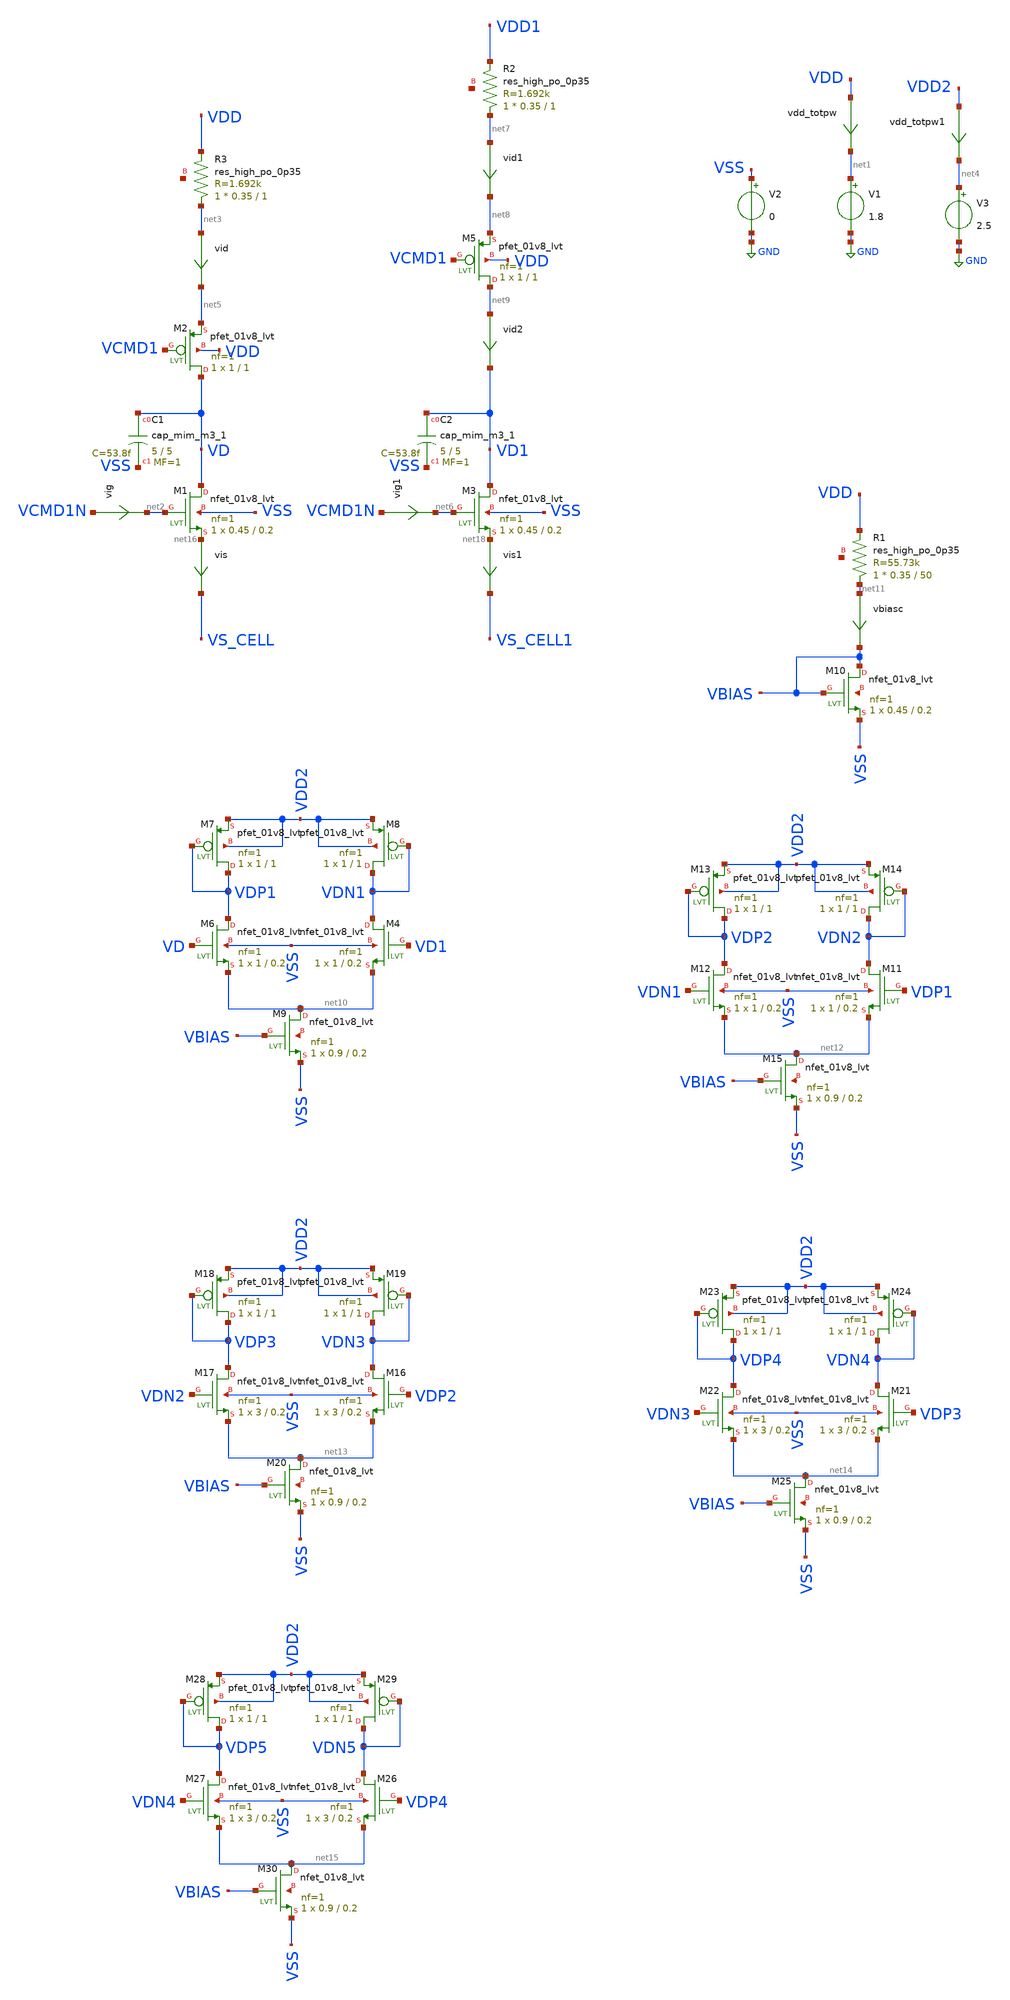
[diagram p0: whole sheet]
** sch_path: xschem/tb_em_dram_cell_sourcecap1.sch
**.subckt tb_em_dram_cell_sourcecap1
V1 net1 GND 1.8
V2 VSS GND 0
vdd_totpw VDD net1 0
.save i(vdd_totpw)
vis net16 VS_CELL 0
.save i(vis)
XR3 net3 VDD net17 sky130_fd_pr__res_high_po_0p35 L=1 mult=1 m=1
vig VCMD1N net2 0
.save i(vig)
vid net3 net5 0
.save i(vid)
XC1 VD VSS sky130_fd_pr__cap_mim_m3_1 W=5 L=5 MF=1 m=1
V3 net4 GND 2.5
vdd_totpw1 VDD2 net4 0
.save i(vdd_totpw1)
XM2 VD VCMD1 net5 VDD sky130_fd_pr__pfet_01v8_lvt L=1 W=1 nf=1 ad='int((nf+1)/2) * W/nf * 0.29' as='int((nf+2)/2) * W/nf * 0.29'
+ pd='2*int((nf+1)/2) * (W/nf + 0.29)' ps='2*int((nf+2)/2) * (W/nf + 0.29)' nrd='0.29 / W' nrs='0.29 / W'
+ sa=0 sb=0 sd=0 mult=1 m=1
vis1 net18 VS_CELL1 0
.save i(vis1)
XR2 net7 VDD1 net19 sky130_fd_pr__res_high_po_0p35 L=1 mult=1 m=1
vig1 VCMD1N net6 0
.save i(vig1)
vid1 net7 net8 0
.save i(vid1)
XC2 VD1 VSS sky130_fd_pr__cap_mim_m3_1 W=5 L=5 MF=1 m=1
XM5 net9 VCMD1 net8 VDD sky130_fd_pr__pfet_01v8_lvt L=1 W=1 nf=1 ad='int((nf+1)/2) * W/nf * 0.29' as='int((nf+2)/2) * W/nf * 0.29'
+ pd='2*int((nf+1)/2) * (W/nf + 0.29)' ps='2*int((nf+2)/2) * (W/nf + 0.29)' nrd='0.29 / W' nrs='0.29 / W'
+ sa=0 sb=0 sd=0 mult=1 m=1
vid2 net9 VD1 0
.save i(vid2)
XM1 VD net2 net16 VSS sky130_fd_pr__nfet_01v8_lvt L=0.2 W=0.45 nf=1 ad=0.4 as=0.4 pd='2*int((nf+1)/2) * (W/nf + 0.29)'
+ ps='2*int((nf+2)/2) * (W/nf + 0.29)' nrd='0.29 / W' nrs='0.29 / W' sa=0 sb=0 sd=0 mult=1 m=1
XM3 VD1 net6 net18 VSS sky130_fd_pr__nfet_01v8_lvt L=0.2 W=0.45 nf=1 ad=0.4 as=0.4 pd='2*int((nf+1)/2) * (W/nf + 0.29)'
+ ps='2*int((nf+2)/2) * (W/nf + 0.29)' nrd='0.29 / W' nrs='0.29 / W' sa=0 sb=0 sd=0 mult=1 m=1
XM4 VDN1 VD1 net10 VSS sky130_fd_pr__nfet_01v8_lvt L=0.2 W=1 nf=1 ad=0.4 as=0.4 pd='2*int((nf+1)/2) * (W/nf + 0.29)'
+ ps='2*int((nf+2)/2) * (W/nf + 0.29)' nrd='0.29 / W' nrs='0.29 / W' sa=0 sb=0 sd=0 mult=1 m=1
XM6 VDP1 VD net10 VSS sky130_fd_pr__nfet_01v8_lvt L=0.2 W=1 nf=1 ad=0.4 as=0.4 pd='2*int((nf+1)/2) * (W/nf + 0.29)'
+ ps='2*int((nf+2)/2) * (W/nf + 0.29)' nrd='0.29 / W' nrs='0.29 / W' sa=0 sb=0 sd=0 mult=1 m=1
XM7 VDP1 VDP1 VDD2 VDD2 sky130_fd_pr__pfet_01v8_lvt L=1 W=1 nf=1 ad='int((nf+1)/2) * W/nf * 0.29' as='int((nf+2)/2) * W/nf * 0.29'
+ pd='2*int((nf+1)/2) * (W/nf + 0.29)' ps='2*int((nf+2)/2) * (W/nf + 0.29)' nrd='0.29 / W' nrs='0.29 / W'
+ sa=0 sb=0 sd=0 mult=1 m=1
XM8 VDN1 VDN1 VDD2 VDD2 sky130_fd_pr__pfet_01v8_lvt L=1 W=1 nf=1 ad='int((nf+1)/2) * W/nf * 0.29' as='int((nf+2)/2) * W/nf * 0.29'
+ pd='2*int((nf+1)/2) * (W/nf + 0.29)' ps='2*int((nf+2)/2) * (W/nf + 0.29)' nrd='0.29 / W' nrs='0.29 / W'
+ sa=0 sb=0 sd=0 mult=1 m=1
XM9 net10 VBIAS VSS net20 sky130_fd_pr__nfet_01v8_lvt L=0.2 W=0.9 nf=1 ad=0.4 as=0.4 pd='2*int((nf+1)/2) * (W/nf + 0.29)'
+ ps='2*int((nf+2)/2) * (W/nf + 0.29)' nrd='0.29 / W' nrs='0.29 / W' sa=0 sb=0 sd=0 mult=1 m=1
XM10 VBIAS VBIAS VSS net21 sky130_fd_pr__nfet_01v8_lvt L=0.2 W=0.45 nf=1 ad=0.4 as=0.4 pd='2*int((nf+1)/2) * (W/nf + 0.29)'
+ ps='2*int((nf+2)/2) * (W/nf + 0.29)' nrd='0.29 / W' nrs='0.29 / W' sa=0 sb=0 sd=0 mult=1 m=1
XR1 net11 VDD net22 sky130_fd_pr__res_high_po_0p35 L=50 mult=1 m=1
vbiasc net11 VBIAS 0
.save i(vbiasc)
XM11 VDN2 VDP1 net12 VSS sky130_fd_pr__nfet_01v8_lvt L=0.2 W=1 nf=1 ad=0.4 as=0.4 pd='2*int((nf+1)/2) * (W/nf + 0.29)'
+ ps='2*int((nf+2)/2) * (W/nf + 0.29)' nrd='0.29 / W' nrs='0.29 / W' sa=0 sb=0 sd=0 mult=1 m=1
XM12 VDP2 VDN1 net12 VSS sky130_fd_pr__nfet_01v8_lvt L=0.2 W=1 nf=1 ad=0.4 as=0.4 pd='2*int((nf+1)/2) * (W/nf + 0.29)'
+ ps='2*int((nf+2)/2) * (W/nf + 0.29)' nrd='0.29 / W' nrs='0.29 / W' sa=0 sb=0 sd=0 mult=1 m=1
XM13 VDP2 VDP2 VDD2 VDD2 sky130_fd_pr__pfet_01v8_lvt L=1 W=1 nf=1 ad='int((nf+1)/2) * W/nf * 0.29' as='int((nf+2)/2) * W/nf * 0.29'
+ pd='2*int((nf+1)/2) * (W/nf + 0.29)' ps='2*int((nf+2)/2) * (W/nf + 0.29)' nrd='0.29 / W' nrs='0.29 / W'
+ sa=0 sb=0 sd=0 mult=1 m=1
XM14 VDN2 VDN2 VDD2 VDD2 sky130_fd_pr__pfet_01v8_lvt L=1 W=1 nf=1 ad='int((nf+1)/2) * W/nf * 0.29' as='int((nf+2)/2) * W/nf * 0.29'
+ pd='2*int((nf+1)/2) * (W/nf + 0.29)' ps='2*int((nf+2)/2) * (W/nf + 0.29)' nrd='0.29 / W' nrs='0.29 / W'
+ sa=0 sb=0 sd=0 mult=1 m=1
XM15 net12 VBIAS VSS net23 sky130_fd_pr__nfet_01v8_lvt L=0.2 W=0.9 nf=1 ad=0.4 as=0.4 pd='2*int((nf+1)/2) * (W/nf + 0.29)'
+ ps='2*int((nf+2)/2) * (W/nf + 0.29)' nrd='0.29 / W' nrs='0.29 / W' sa=0 sb=0 sd=0 mult=1 m=1
XM16 VDN3 VDP2 net13 VSS sky130_fd_pr__nfet_01v8_lvt L=0.2 W=3 nf=1 ad=0.4 as=0.4 pd='2*int((nf+1)/2) * (W/nf + 0.29)'
+ ps='2*int((nf+2)/2) * (W/nf + 0.29)' nrd='0.29 / W' nrs='0.29 / W' sa=0 sb=0 sd=0 mult=1 m=1
XM17 VDP3 VDN2 net13 VSS sky130_fd_pr__nfet_01v8_lvt L=0.2 W=3 nf=1 ad=0.4 as=0.4 pd='2*int((nf+1)/2) * (W/nf + 0.29)'
+ ps='2*int((nf+2)/2) * (W/nf + 0.29)' nrd='0.29 / W' nrs='0.29 / W' sa=0 sb=0 sd=0 mult=1 m=1
XM18 VDP3 VDP3 VDD2 VDD2 sky130_fd_pr__pfet_01v8_lvt L=1 W=1 nf=1 ad='int((nf+1)/2) * W/nf * 0.29' as='int((nf+2)/2) * W/nf * 0.29'
+ pd='2*int((nf+1)/2) * (W/nf + 0.29)' ps='2*int((nf+2)/2) * (W/nf + 0.29)' nrd='0.29 / W' nrs='0.29 / W'
+ sa=0 sb=0 sd=0 mult=1 m=1
XM19 VDN3 VDN3 VDD2 VDD2 sky130_fd_pr__pfet_01v8_lvt L=1 W=1 nf=1 ad='int((nf+1)/2) * W/nf * 0.29' as='int((nf+2)/2) * W/nf * 0.29'
+ pd='2*int((nf+1)/2) * (W/nf + 0.29)' ps='2*int((nf+2)/2) * (W/nf + 0.29)' nrd='0.29 / W' nrs='0.29 / W'
+ sa=0 sb=0 sd=0 mult=1 m=1
XM20 net13 VBIAS VSS net24 sky130_fd_pr__nfet_01v8_lvt L=0.2 W=0.9 nf=1 ad=0.4 as=0.4 pd='2*int((nf+1)/2) * (W/nf + 0.29)'
+ ps='2*int((nf+2)/2) * (W/nf + 0.29)' nrd='0.29 / W' nrs='0.29 / W' sa=0 sb=0 sd=0 mult=1 m=1
XM21 VDN4 VDP3 net14 VSS sky130_fd_pr__nfet_01v8_lvt L=0.2 W=3 nf=1 ad=0.4 as=0.4 pd='2*int((nf+1)/2) * (W/nf + 0.29)'
+ ps='2*int((nf+2)/2) * (W/nf + 0.29)' nrd='0.29 / W' nrs='0.29 / W' sa=0 sb=0 sd=0 mult=1 m=1
XM22 VDP4 VDN3 net14 VSS sky130_fd_pr__nfet_01v8_lvt L=0.2 W=3 nf=1 ad=0.4 as=0.4 pd='2*int((nf+1)/2) * (W/nf + 0.29)'
+ ps='2*int((nf+2)/2) * (W/nf + 0.29)' nrd='0.29 / W' nrs='0.29 / W' sa=0 sb=0 sd=0 mult=1 m=1
XM23 VDP4 VDP4 VDD2 VDD2 sky130_fd_pr__pfet_01v8_lvt L=1 W=1 nf=1 ad='int((nf+1)/2) * W/nf * 0.29' as='int((nf+2)/2) * W/nf * 0.29'
+ pd='2*int((nf+1)/2) * (W/nf + 0.29)' ps='2*int((nf+2)/2) * (W/nf + 0.29)' nrd='0.29 / W' nrs='0.29 / W'
+ sa=0 sb=0 sd=0 mult=1 m=1
XM24 VDN4 VDN4 VDD2 VDD2 sky130_fd_pr__pfet_01v8_lvt L=1 W=1 nf=1 ad='int((nf+1)/2) * W/nf * 0.29' as='int((nf+2)/2) * W/nf * 0.29'
+ pd='2*int((nf+1)/2) * (W/nf + 0.29)' ps='2*int((nf+2)/2) * (W/nf + 0.29)' nrd='0.29 / W' nrs='0.29 / W'
+ sa=0 sb=0 sd=0 mult=1 m=1
XM25 net14 VBIAS VSS net25 sky130_fd_pr__nfet_01v8_lvt L=0.2 W=0.9 nf=1 ad=0.4 as=0.4 pd='2*int((nf+1)/2) * (W/nf + 0.29)'
+ ps='2*int((nf+2)/2) * (W/nf + 0.29)' nrd='0.29 / W' nrs='0.29 / W' sa=0 sb=0 sd=0 mult=1 m=1
XM26 VDN5 VDP4 net15 VSS sky130_fd_pr__nfet_01v8_lvt L=0.2 W=3 nf=1 ad=0.4 as=0.4 pd='2*int((nf+1)/2) * (W/nf + 0.29)'
+ ps='2*int((nf+2)/2) * (W/nf + 0.29)' nrd='0.29 / W' nrs='0.29 / W' sa=0 sb=0 sd=0 mult=1 m=1
XM27 VDP5 VDN4 net15 VSS sky130_fd_pr__nfet_01v8_lvt L=0.2 W=3 nf=1 ad=0.4 as=0.4 pd='2*int((nf+1)/2) * (W/nf + 0.29)'
+ ps='2*int((nf+2)/2) * (W/nf + 0.29)' nrd='0.29 / W' nrs='0.29 / W' sa=0 sb=0 sd=0 mult=1 m=1
XM28 VDP5 VDP5 VDD2 VDD2 sky130_fd_pr__pfet_01v8_lvt L=1 W=1 nf=1 ad='int((nf+1)/2) * W/nf * 0.29' as='int((nf+2)/2) * W/nf * 0.29'
+ pd='2*int((nf+1)/2) * (W/nf + 0.29)' ps='2*int((nf+2)/2) * (W/nf + 0.29)' nrd='0.29 / W' nrs='0.29 / W'
+ sa=0 sb=0 sd=0 mult=1 m=1
XM29 VDN5 VDN5 VDD2 VDD2 sky130_fd_pr__pfet_01v8_lvt L=1 W=1 nf=1 ad='int((nf+1)/2) * W/nf * 0.29' as='int((nf+2)/2) * W/nf * 0.29'
+ pd='2*int((nf+1)/2) * (W/nf + 0.29)' ps='2*int((nf+2)/2) * (W/nf + 0.29)' nrd='0.29 / W' nrs='0.29 / W'
+ sa=0 sb=0 sd=0 mult=1 m=1
XM30 net15 VBIAS VSS net26 sky130_fd_pr__nfet_01v8_lvt L=0.2 W=0.9 nf=1 ad=0.4 as=0.4 pd='2*int((nf+1)/2) * (W/nf + 0.29)'
+ ps='2*int((nf+2)/2) * (W/nf + 0.29)' nrd='0.29 / W' nrs='0.29 / W' sa=0 sb=0 sd=0 mult=1 m=1
**** begin user architecture code

** opencircuitdesign pdks install
.lib $::SKYWATER_MODELS/sky130.lib.spice tt
*.lib $::SKYWATER_STDCELLS/sky130_fd_sc_hd_blablabla.spice

.subckt sky130_fd_sc_hd__inv_1 A VGND VNB VPB VPWR Y
X0 VGND A Y VNB sky130_fd_pr__nfet_01v8 w=650000u l=150000u
X1 VPWR A Y VPB sky130_fd_pr__pfet_01v8_hvt w=1e+06u l=150000u
.ends





.options savecurrents
* VCMD2 VCMD2   0 pulse 1.8 1.2 20u 1n 1n 700u 1400u
VCMD2 VCMD2   0 sine  0.9 0.9  10k 0 0
VCMD1N VCMD1N 0 pulse 0   1.8 6u 1n 1n 50n 20u
VCMD1 VCMD1   0 pulse 1.8 0 5u 1n 1n 5u 60u
VDD1 VDD1     0 pulse 1.8 0 4u 1n 1n 4u 60u
* VCMD0 VCMD0   0 sine  0.9 0.9  100meg 0 0
* VCMD1 VCMD1   0 pulse 1.8   0 7u 1n 1n 5u 10m
* VCMD0 VCMD0   0 pulse 1.20 1.10 0n 1n 1n 50n  100n
* VCMD1X VCMD1X   0 pulse 1.8 1.7 0.5m 1p 1p 5u  10u
* VCMD2X VCMD2X   0 pulse 0 1.8 0.5m 1p 1p 5u  10u
.control
  repeat 1
    save all
    tran 0.1n 50u
    remzerovec
    write tb_em_dram_cell_sourcecap1.raw
    set appendwrite
    reset
    end
.endc



**** end user architecture code
**.ends
.GLOBAL GND
.end
